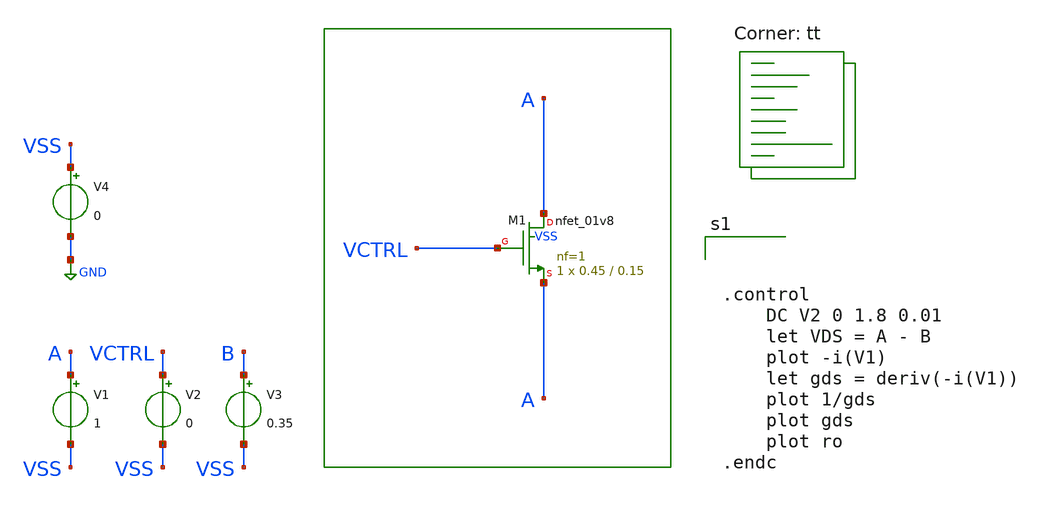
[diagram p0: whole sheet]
** sch_path: CTLE/passives-characterization/active-resistor.sch
**.subckt active-resistor
XM1 A VCTRL A VSS sky130_fd_pr__nfet_01v8 L=0.15 W=0.45 nf=1 ad='int((nf+1)/2) * W/nf * 0.29' as='int((nf+2)/2) * W/nf * 0.29'
+ pd='2*int((nf+1)/2) * (W/nf + 0.29)' ps='2*int((nf+2)/2) * (W/nf + 0.29)' nrd='0.29 / W' nrs='0.29 / W'
+ sa=0 sb=0 sd=0 mult=1 m=1
V1 A VSS 1
V2 VCTRL VSS 0
V3 B VSS 0.35
V4 VSS GND 0
**** begin user architecture code
.lib $::SKYWATER_MODELS/sky130.lib.spice tt



.control
	DC V2 0 1.8 0.01
	let VDS = A - B
	plot -i(V1)
	let gds = deriv(-i(V1))
	plot 1/gds
	plot gds
	plot ro
.endc



**** end user architecture code
**.ends
.GLOBAL GND
.end
